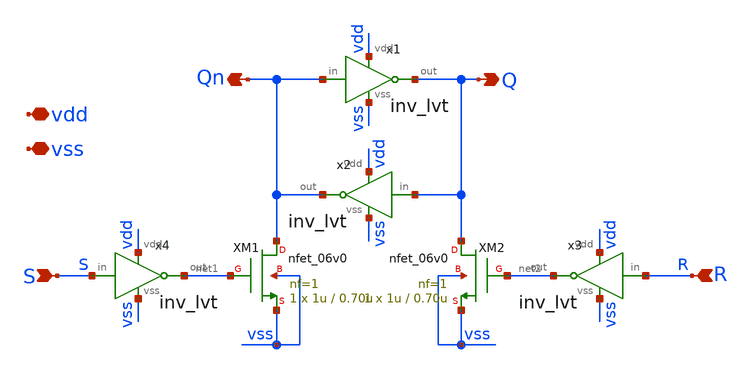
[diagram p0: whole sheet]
** sch_path: check/xschem/sar_10b/latch/latch.sch
**.subckt latch S R vss vdd Q Qn
*.ipin S
*.ipin R
*.iopin vss
*.iopin vdd
*.opin Q
*.opin Qn
x1 vdd Qn Q vss inv_lvt
x2 vdd Q Qn vss inv_lvt
x3 vdd R net2 vss inv_lvt
x4 vdd S net1 vss inv_lvt
XM1 Qn net1 vss vss nfet_06v0 L=0.70u W=1u nf=1 ad='int((nf+1)/2) * W/nf * 0.18u' as='int((nf+2)/2) * W/nf * 0.18u'
+ pd='2*int((nf+1)/2) * (W/nf + 0.18u)' ps='2*int((nf+2)/2) * (W/nf + 0.18u)' nrd='0.18u / W' nrs='0.18u / W'
+ sa=0 sb=0 sd=0 m=1
XM2 Q net2 vss vss nfet_06v0 L=0.70u W=1u nf=1 ad='int((nf+1)/2) * W/nf * 0.18u' as='int((nf+2)/2) * W/nf * 0.18u'
+ pd='2*int((nf+1)/2) * (W/nf + 0.18u)' ps='2*int((nf+2)/2) * (W/nf + 0.18u)' nrd='0.18u / W' nrs='0.18u / W'
+ sa=0 sb=0 sd=0 m=1
**.ends

* expanding   symbol:  logic/inv_lvt.sym # of pins=4
** sym_path: logic/inv_lvt.sym
** sch_path: logic/inv_lvt.sch
.subckt inv_lvt vdd in out vss
*.iopin vdd
*.iopin vss
*.ipin in
*.opin out
XM1 out in vss vss nfet_06v0 L=0.70u W=1u nf=1 ad='int((nf+1)/2) * W/nf * 0.18u' as='int((nf+2)/2) * W/nf * 0.18u'
+ pd='2*int((nf+1)/2) * (W/nf + 0.18u)' ps='2*int((nf+2)/2) * (W/nf + 0.18u)' nrd='0.18u / W' nrs='0.18u / W'
+ sa=0 sb=0 sd=0 m=1
XM2 out in vdd vdd pfet_06v0 L=0.55u W=1u nf=1 ad='int((nf+1)/2) * W/nf * 0.18u' as='int((nf+2)/2) * W/nf * 0.18u'
+ pd='2*int((nf+1)/2) * (W/nf + 0.18u)' ps='2*int((nf+2)/2) * (W/nf + 0.18u)' nrd='0.18u / W' nrs='0.18u / W'
+ sa=0 sb=0 sd=0 m=1
.ends

.end
